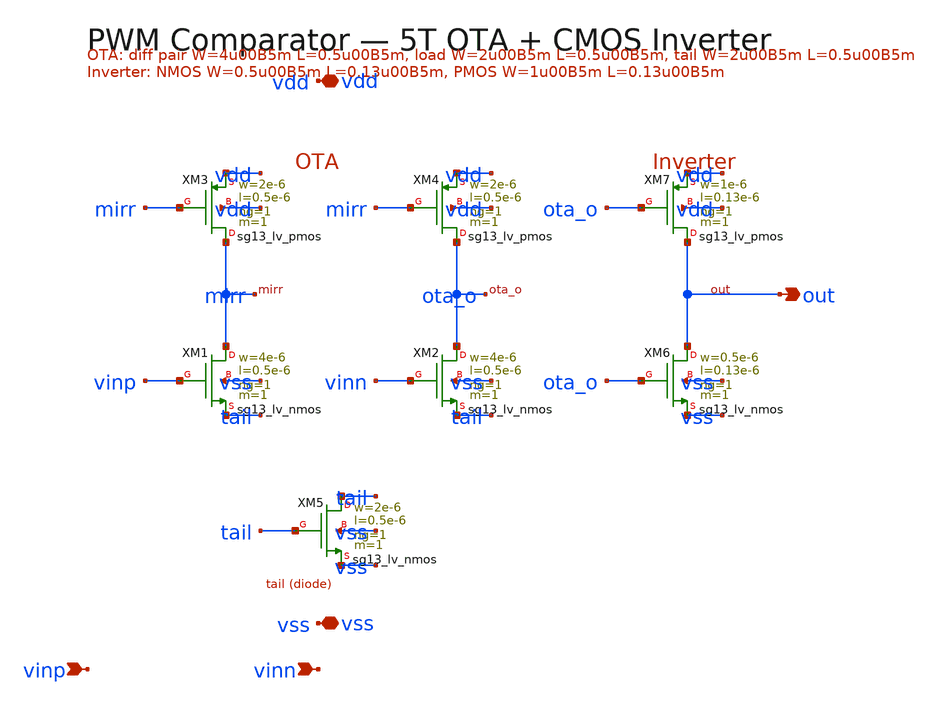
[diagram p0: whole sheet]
** sch_path: xschem/pwm_comp.sch
**.subckt pwm_comp vdd vss vinp vinn out
*.iopin vdd
*.iopin vss
*.ipin vinp
*.ipin vinn
*.opin out
XXM3 mirr mirr vdd vdd sg13_lv_pmos w=2e-6 l=0.5e-6 ng=1 m=1 mm_ok=1
XXM4 ota_o mirr vdd vdd sg13_lv_pmos w=2e-6 l=0.5e-6 ng=1 m=1 mm_ok=1
XXM1 mirr vinp tail vss sg13_lv_nmos w=4e-6 l=0.5e-6 ng=1 m=1 mm_ok=1
XXM2 ota_o vinn tail vss sg13_lv_nmos w=4e-6 l=0.5e-6 ng=1 m=1 mm_ok=1
XXM5 tail tail vss vss sg13_lv_nmos w=2e-6 l=0.5e-6 ng=1 m=1 mm_ok=1
XXM7 out ota_o vdd vdd sg13_lv_pmos w=1e-6 l=0.13e-6 ng=1 m=1 mm_ok=1
XXM6 out ota_o vss vss sg13_lv_nmos w=0.5e-6 l=0.13e-6 ng=1 m=1 mm_ok=1
**.ends
.end
